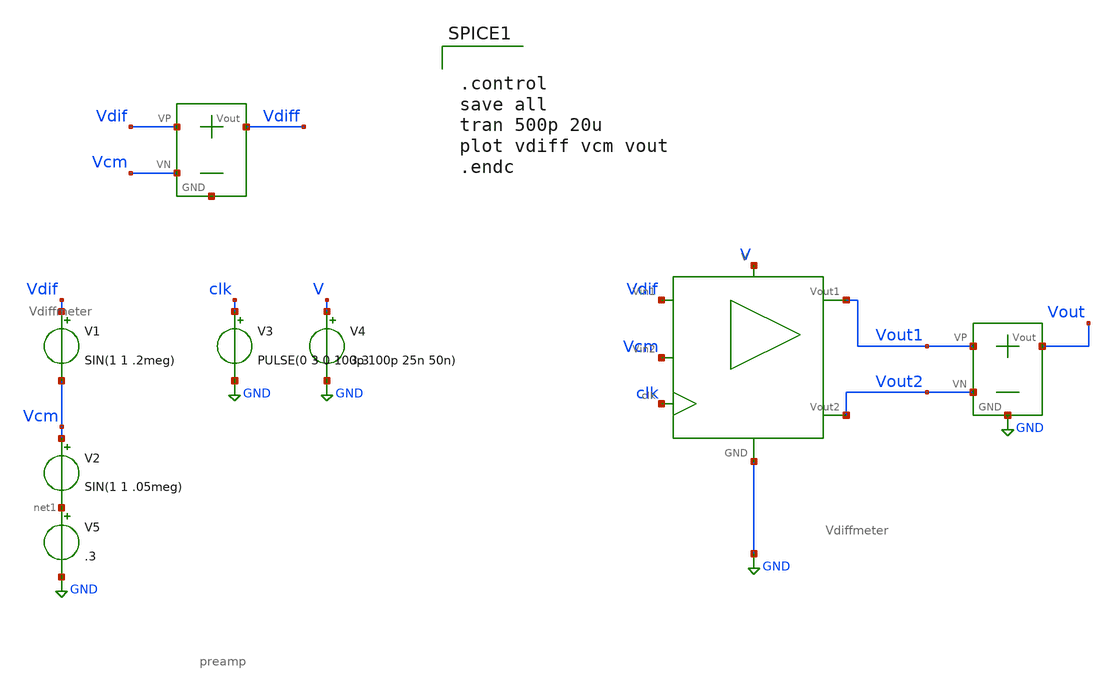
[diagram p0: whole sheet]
** sch_path: SAR_ADC/xschem/test/preamp_tb/vdif_sin-vcm_sin__tb.sch
**.subckt vdif_sin-vcm_sin__tb
V1 Vdif Vcm SIN(1 1 .2meg)
V2 Vcm net1 SIN(1 1 .05meg)
V3 clk GND PULSE(0 3 0 100p 100p 25n 50n)
V4 V GND 3.3
X1 V GND Vdif clk Vout1 Vout2 Vcm preamp
X3 Vout1 Vout2 Vout GND Vdiffmeter
X2 Vdif Vcm Vdiff net2 Vdiffmeter
V5 net1 GND .3
**** begin user architecture code


.control
save all
tran 500p 20u
plot vdiff vcm vout
.endc


.include /foss/pdks/gf180mcuC/libs.tech/ngspice/design.ngspice
.lib /foss/pdks/gf180mcuC/libs.tech/ngspice/sm141064.ngspice typical

**** end user architecture code
**.ends
.GLOBAL GND
.end
